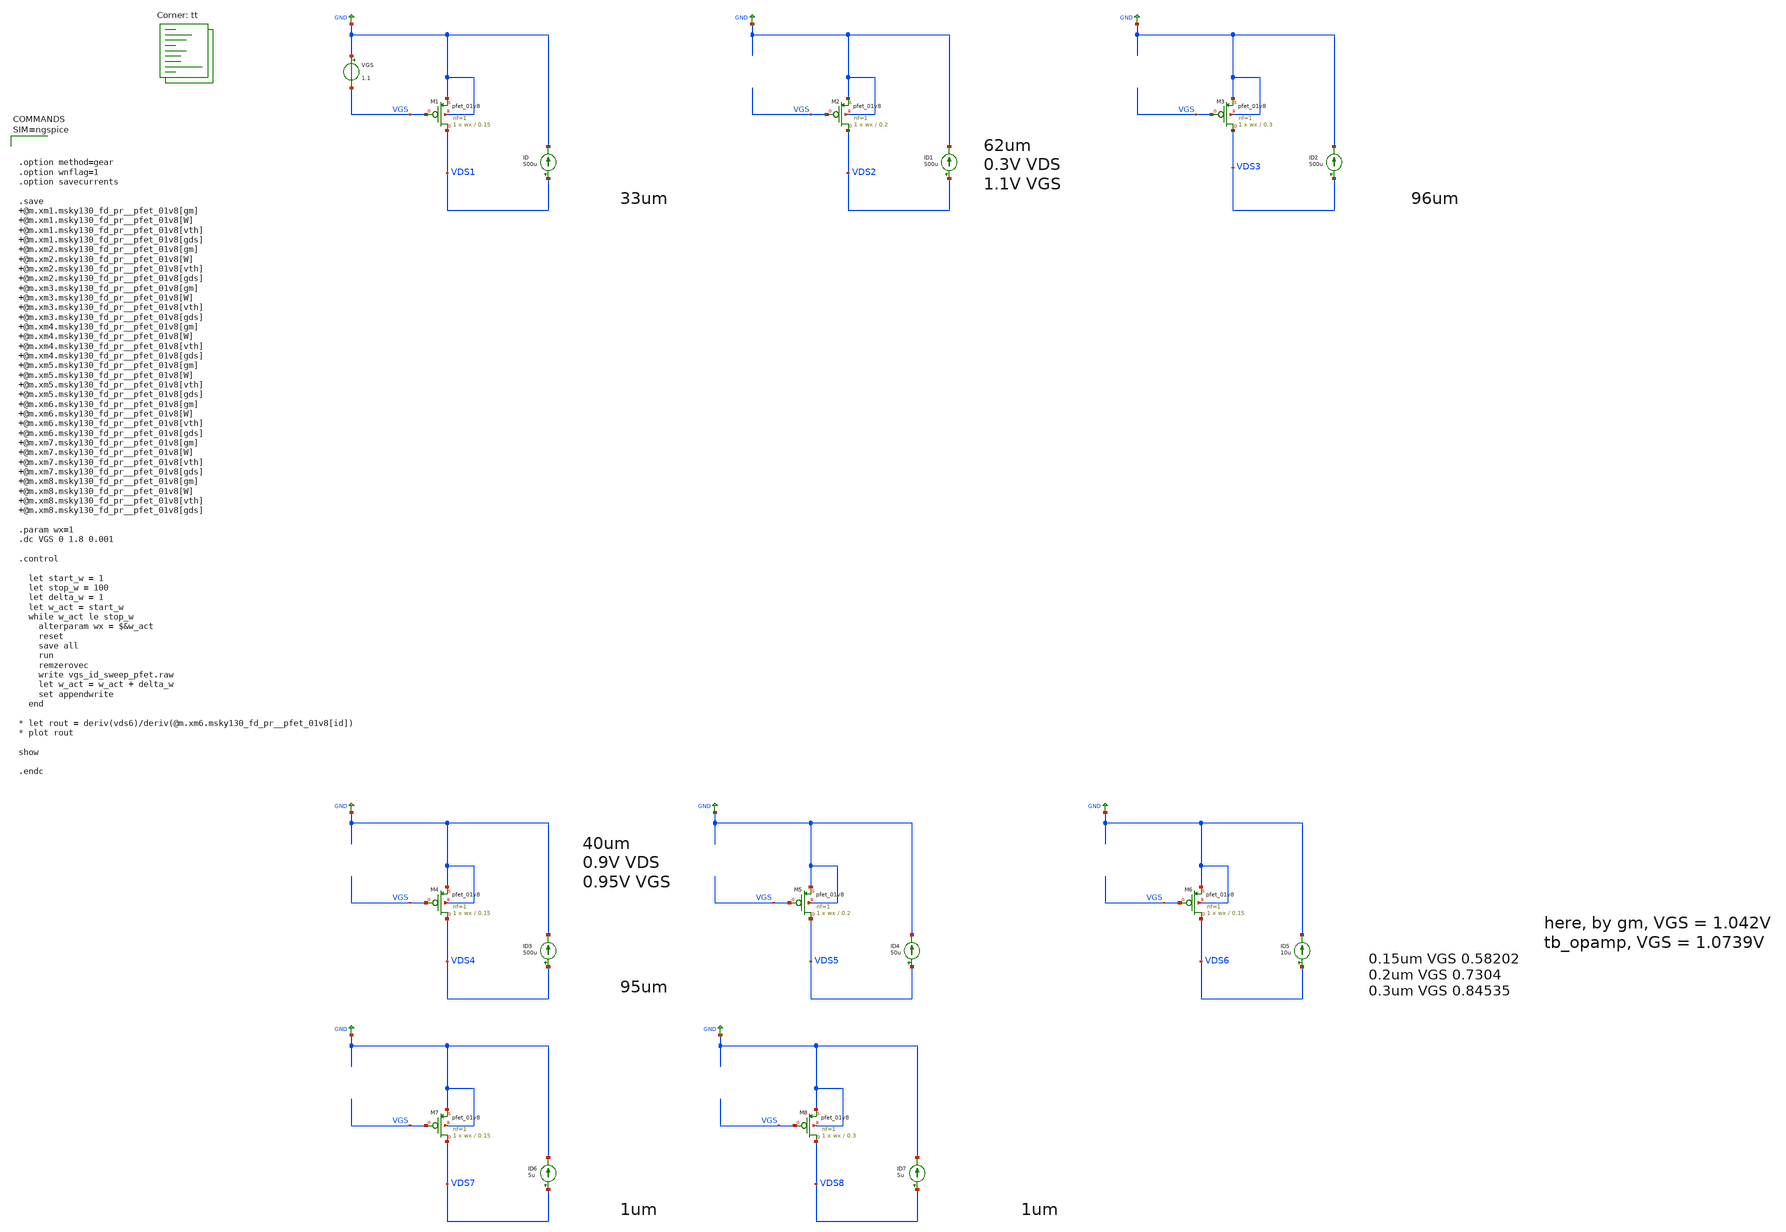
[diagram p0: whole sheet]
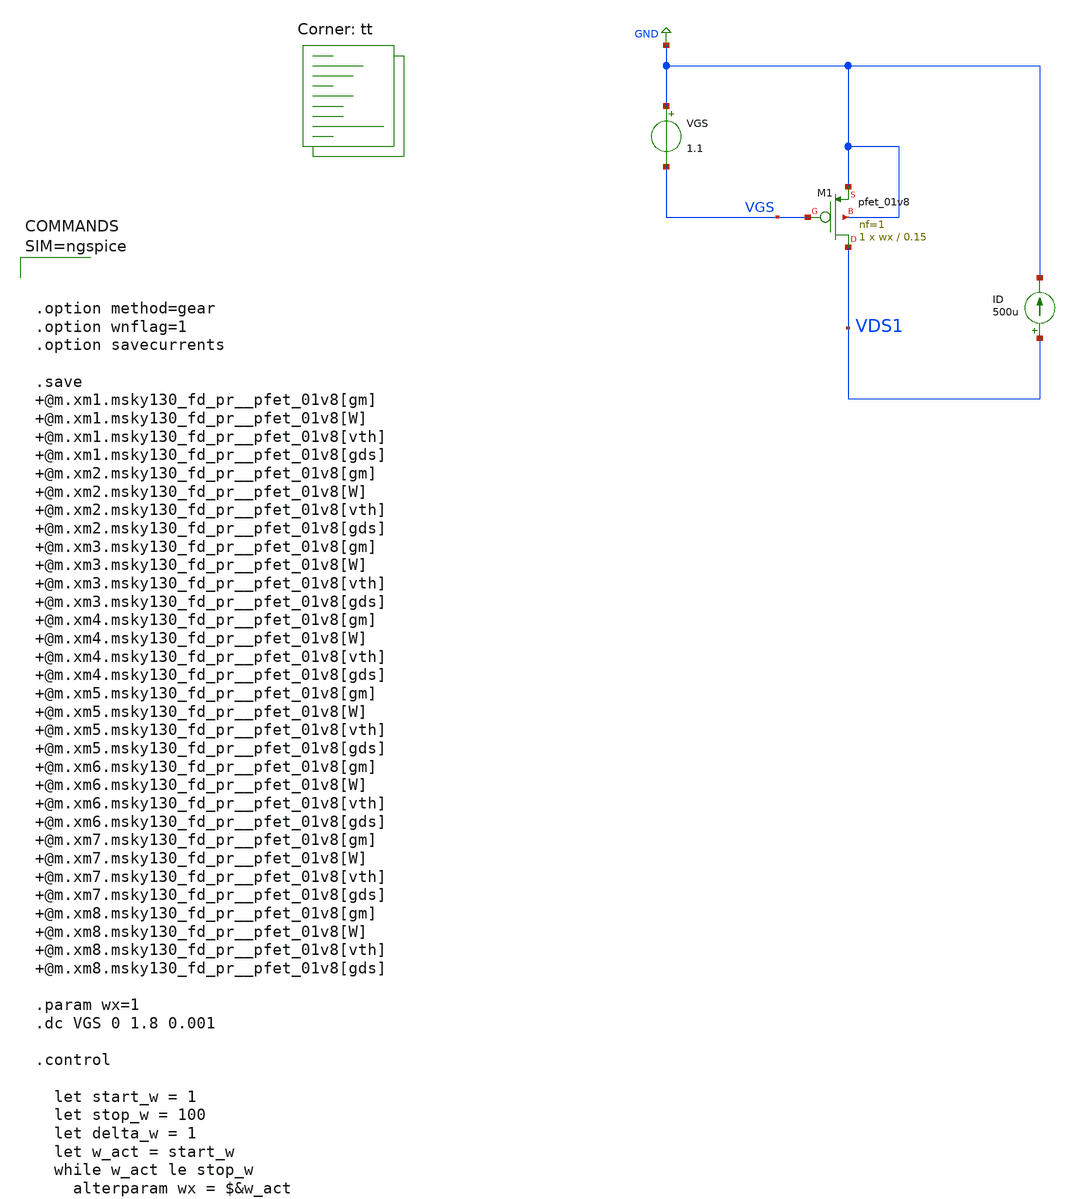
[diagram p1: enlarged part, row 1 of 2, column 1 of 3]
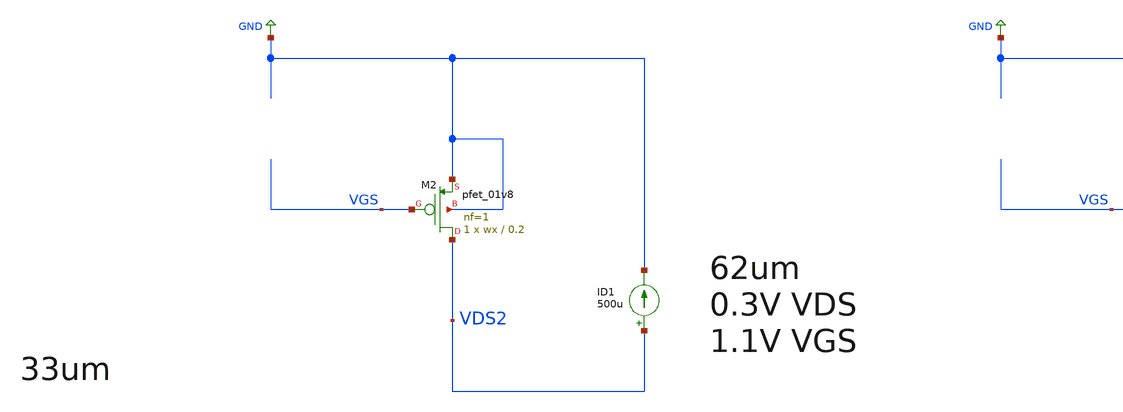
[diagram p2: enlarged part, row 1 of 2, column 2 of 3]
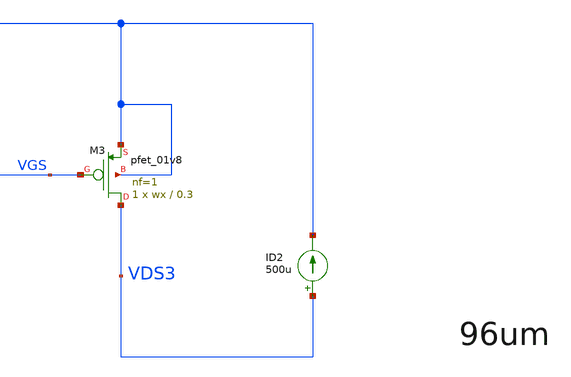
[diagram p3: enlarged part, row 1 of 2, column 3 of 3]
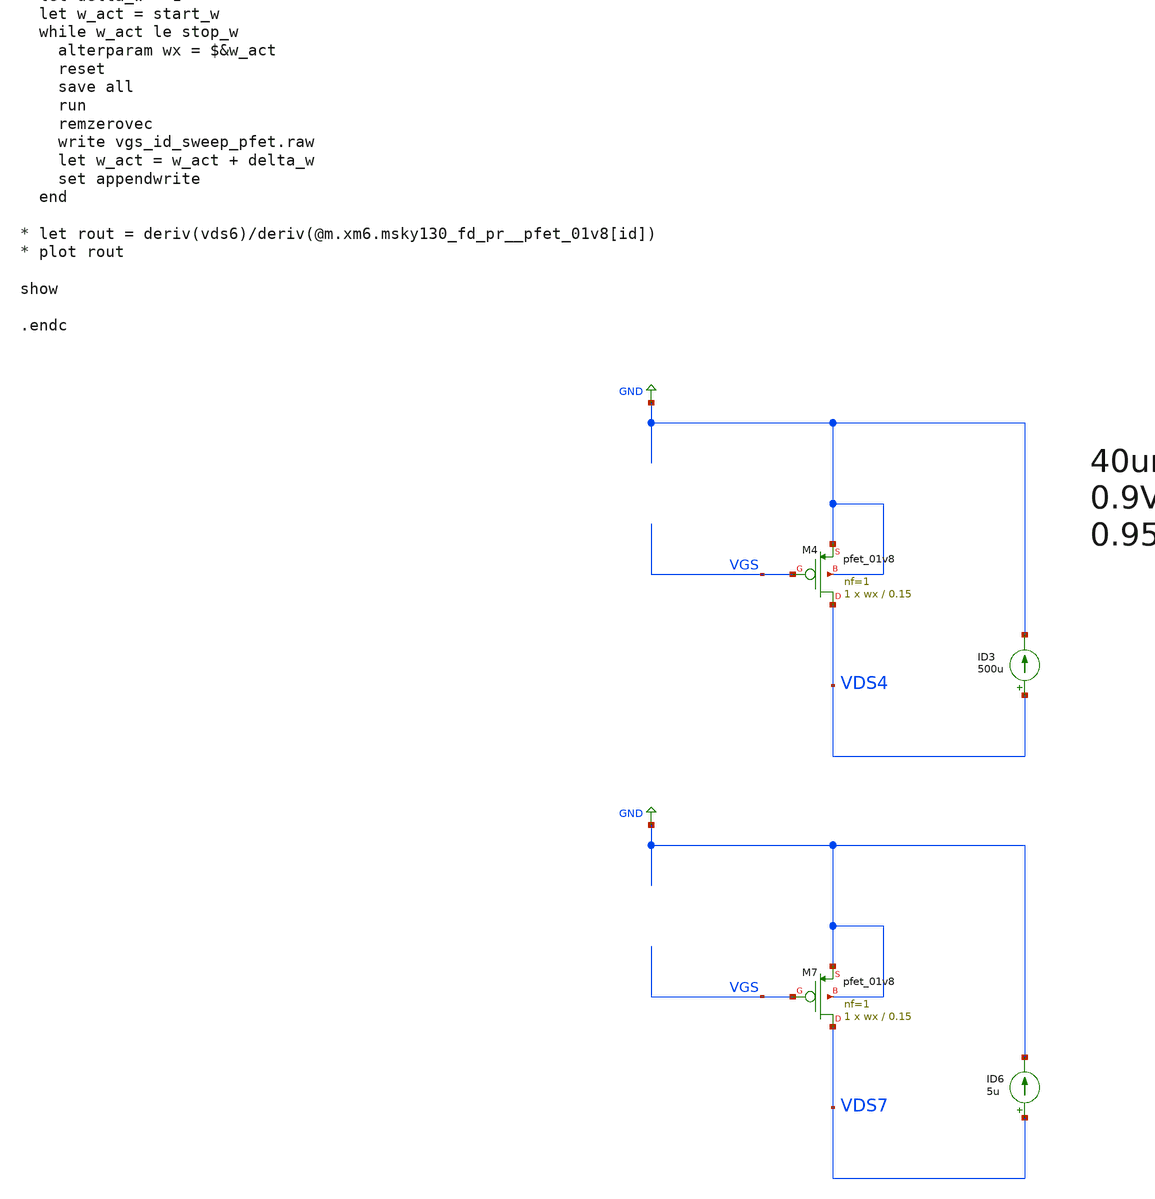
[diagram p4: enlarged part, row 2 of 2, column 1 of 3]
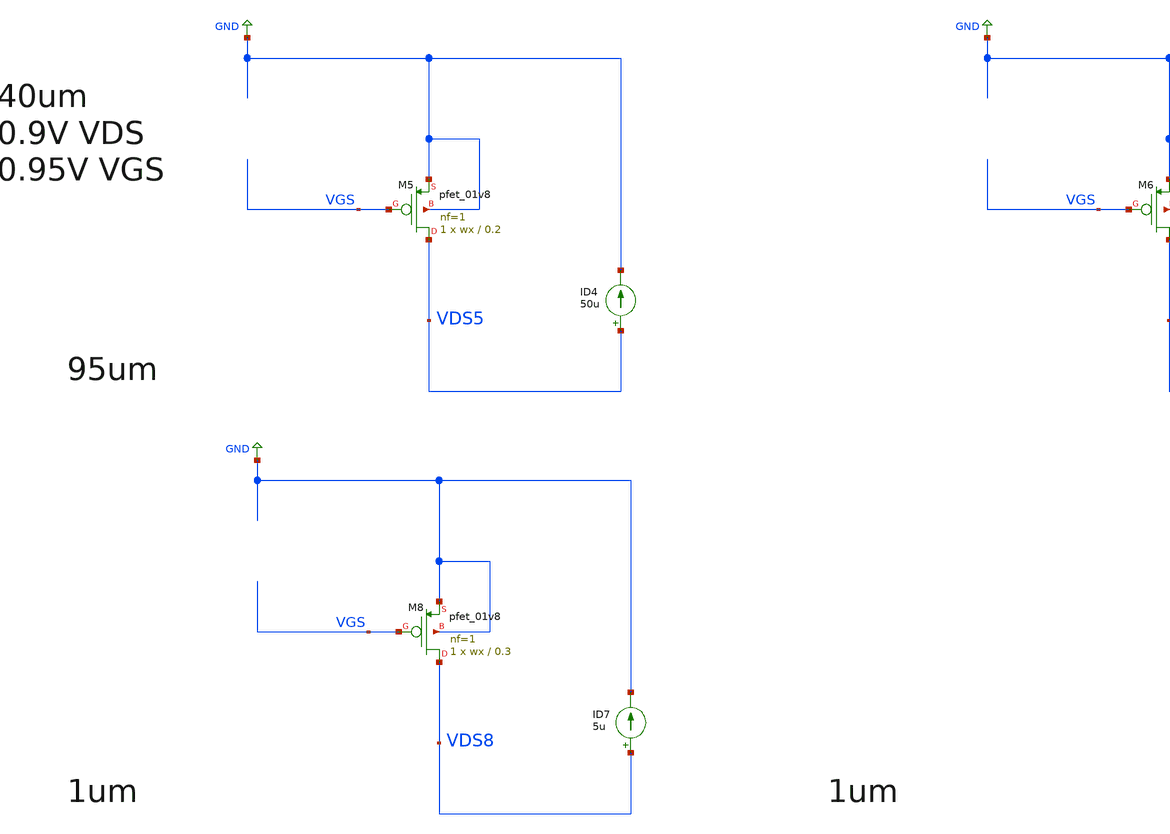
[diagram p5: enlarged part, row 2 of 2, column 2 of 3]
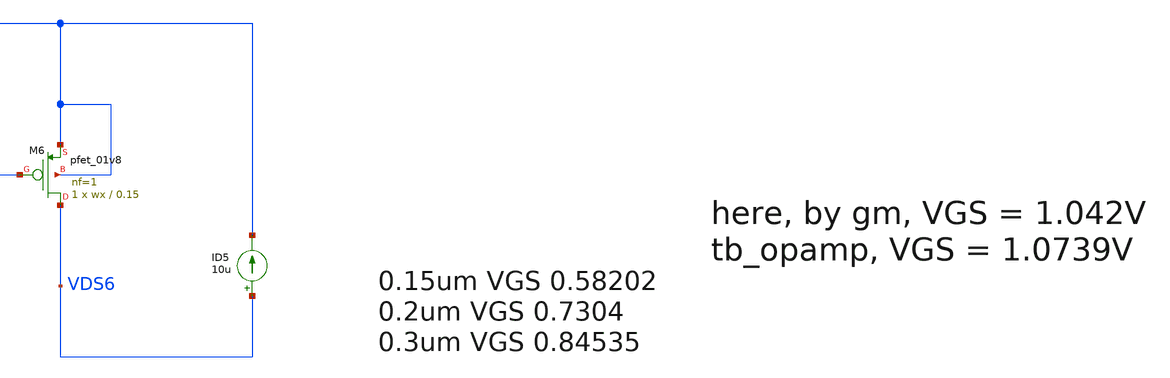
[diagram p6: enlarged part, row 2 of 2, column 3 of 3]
** sch_path: projects/opamp/xschem_ngspice/vgs_id_sweep_pfet.sch
**.subckt vgs_id_sweep_pfet
VGS GND VGS 1.1
ID VDS1 GND 500u
XM1 VDS1 VGS GND GND sky130_fd_pr__pfet_01v8 L=0.15 W=wx nf=1 ad='int((nf+1)/2) * W/nf * 0.29' as='int((nf+2)/2) * W/nf * 0.29'
+ pd='2*int((nf+1)/2) * (W/nf + 0.29)' ps='2*int((nf+2)/2) * (W/nf + 0.29)' nrd='0.29 / W' nrs='0.29 / W'
+ sa=0 sb=0 sd=0 mult=1 m=1
ID1 VDS2 GND 500u
XM2 VDS2 VGS GND GND sky130_fd_pr__pfet_01v8 L=0.2 W=wx nf=1 ad='int((nf+1)/2) * W/nf * 0.29' as='int((nf+2)/2) * W/nf * 0.29'
+ pd='2*int((nf+1)/2) * (W/nf + 0.29)' ps='2*int((nf+2)/2) * (W/nf + 0.29)' nrd='0.29 / W' nrs='0.29 / W'
+ sa=0 sb=0 sd=0 mult=1 m=1
ID2 VDS3 GND 500u
XM3 VDS3 VGS GND GND sky130_fd_pr__pfet_01v8 L=0.3 W=wx nf=1 ad='int((nf+1)/2) * W/nf * 0.29' as='int((nf+2)/2) * W/nf * 0.29'
+ pd='2*int((nf+1)/2) * (W/nf + 0.29)' ps='2*int((nf+2)/2) * (W/nf + 0.29)' nrd='0.29 / W' nrs='0.29 / W'
+ sa=0 sb=0 sd=0 mult=1 m=1
ID3 VDS4 GND 500u
XM4 VDS4 VGS GND GND sky130_fd_pr__pfet_01v8 L=0.15 W=wx nf=1 ad='int((nf+1)/2) * W/nf * 0.29' as='int((nf+2)/2) * W/nf * 0.29'
+ pd='2*int((nf+1)/2) * (W/nf + 0.29)' ps='2*int((nf+2)/2) * (W/nf + 0.29)' nrd='0.29 / W' nrs='0.29 / W'
+ sa=0 sb=0 sd=0 mult=1 m=1
ID4 VDS5 GND 50u
XM5 VDS5 VGS GND GND sky130_fd_pr__pfet_01v8 L=0.2 W=wx nf=1 ad='int((nf+1)/2) * W/nf * 0.29' as='int((nf+2)/2) * W/nf * 0.29'
+ pd='2*int((nf+1)/2) * (W/nf + 0.29)' ps='2*int((nf+2)/2) * (W/nf + 0.29)' nrd='0.29 / W' nrs='0.29 / W'
+ sa=0 sb=0 sd=0 mult=1 m=1
ID5 VDS6 GND 10u
XM6 VDS6 VGS GND GND sky130_fd_pr__pfet_01v8 L=0.15 W=wx nf=1 ad='int((nf+1)/2) * W/nf * 0.29' as='int((nf+2)/2) * W/nf * 0.29'
+ pd='2*int((nf+1)/2) * (W/nf + 0.29)' ps='2*int((nf+2)/2) * (W/nf + 0.29)' nrd='0.29 / W' nrs='0.29 / W'
+ sa=0 sb=0 sd=0 mult=1 m=1
ID6 VDS7 GND 5u
XM7 VDS7 VGS GND GND sky130_fd_pr__pfet_01v8 L=0.15 W=wx nf=1 ad='int((nf+1)/2) * W/nf * 0.29' as='int((nf+2)/2) * W/nf * 0.29'
+ pd='2*int((nf+1)/2) * (W/nf + 0.29)' ps='2*int((nf+2)/2) * (W/nf + 0.29)' nrd='0.29 / W' nrs='0.29 / W'
+ sa=0 sb=0 sd=0 mult=1 m=1
ID7 VDS8 GND 5u
XM8 VDS8 VGS GND GND sky130_fd_pr__pfet_01v8 L=0.3 W=wx nf=1 ad='int((nf+1)/2) * W/nf * 0.29' as='int((nf+2)/2) * W/nf * 0.29'
+ pd='2*int((nf+1)/2) * (W/nf + 0.29)' ps='2*int((nf+2)/2) * (W/nf + 0.29)' nrd='0.29 / W' nrs='0.29 / W'
+ sa=0 sb=0 sd=0 mult=1 m=1
**** begin user architecture code
.lib $::SKYWATER_MODELS/sky130.lib.spice tt




.option method=gear
.option wnflag=1
.option savecurrents

.save @m.xm1.msky130_fd_pr__pfet_01v8[gm] @m.xm1.msky130_fd_pr__pfet_01v8[W] @m.xm1.msky130_fd_pr__pfet_01v8[vth] @m.xm1.msky130_fd_pr__pfet_01v8[gds] @m.xm2.msky130_fd_pr__pfet_01v8[gm] @m.xm2.msky130_fd_pr__pfet_01v8[W] @m.xm2.msky130_fd_pr__pfet_01v8[vth] @m.xm2.msky130_fd_pr__pfet_01v8[gds] @m.xm3.msky130_fd_pr__pfet_01v8[gm] @m.xm3.msky130_fd_pr__pfet_01v8[W] @m.xm3.msky130_fd_pr__pfet_01v8[vth] @m.xm3.msky130_fd_pr__pfet_01v8[gds] @m.xm4.msky130_fd_pr__pfet_01v8[gm] @m.xm4.msky130_fd_pr__pfet_01v8[W] @m.xm4.msky130_fd_pr__pfet_01v8[vth] @m.xm4.msky130_fd_pr__pfet_01v8[gds] @m.xm5.msky130_fd_pr__pfet_01v8[gm] @m.xm5.msky130_fd_pr__pfet_01v8[W] @m.xm5.msky130_fd_pr__pfet_01v8[vth] @m.xm5.msky130_fd_pr__pfet_01v8[gds] @m.xm6.msky130_fd_pr__pfet_01v8[gm] @m.xm6.msky130_fd_pr__pfet_01v8[W] @m.xm6.msky130_fd_pr__pfet_01v8[vth] @m.xm6.msky130_fd_pr__pfet_01v8[gds] @m.xm7.msky130_fd_pr__pfet_01v8[gm] @m.xm7.msky130_fd_pr__pfet_01v8[W] @m.xm7.msky130_fd_pr__pfet_01v8[vth] @m.xm7.msky130_fd_pr__pfet_01v8[gds] @m.xm8.msky130_fd_pr__pfet_01v8[gm] @m.xm8.msky130_fd_pr__pfet_01v8[W] @m.xm8.msky130_fd_pr__pfet_01v8[vth] @m.xm8.msky130_fd_pr__pfet_01v8[gds]

.param wx=1
.dc VGS 0 1.8 0.001

.control

  let start_w = 1
  let stop_w = 100
  let delta_w = 1
  let w_act = start_w
  while w_act le stop_w
    alterparam wx = $&w_act
    reset
    save all
    run
    remzerovec
    write vgs_id_sweep_pfet.raw
    let w_act = w_act + delta_w
    set appendwrite
  end

* let rout = deriv(vds6)/deriv(@m.xm6.msky130_fd_pr__pfet_01v8[id])
* plot rout

show

.endc




**** end user architecture code
**.ends
.GLOBAL GND
.end
